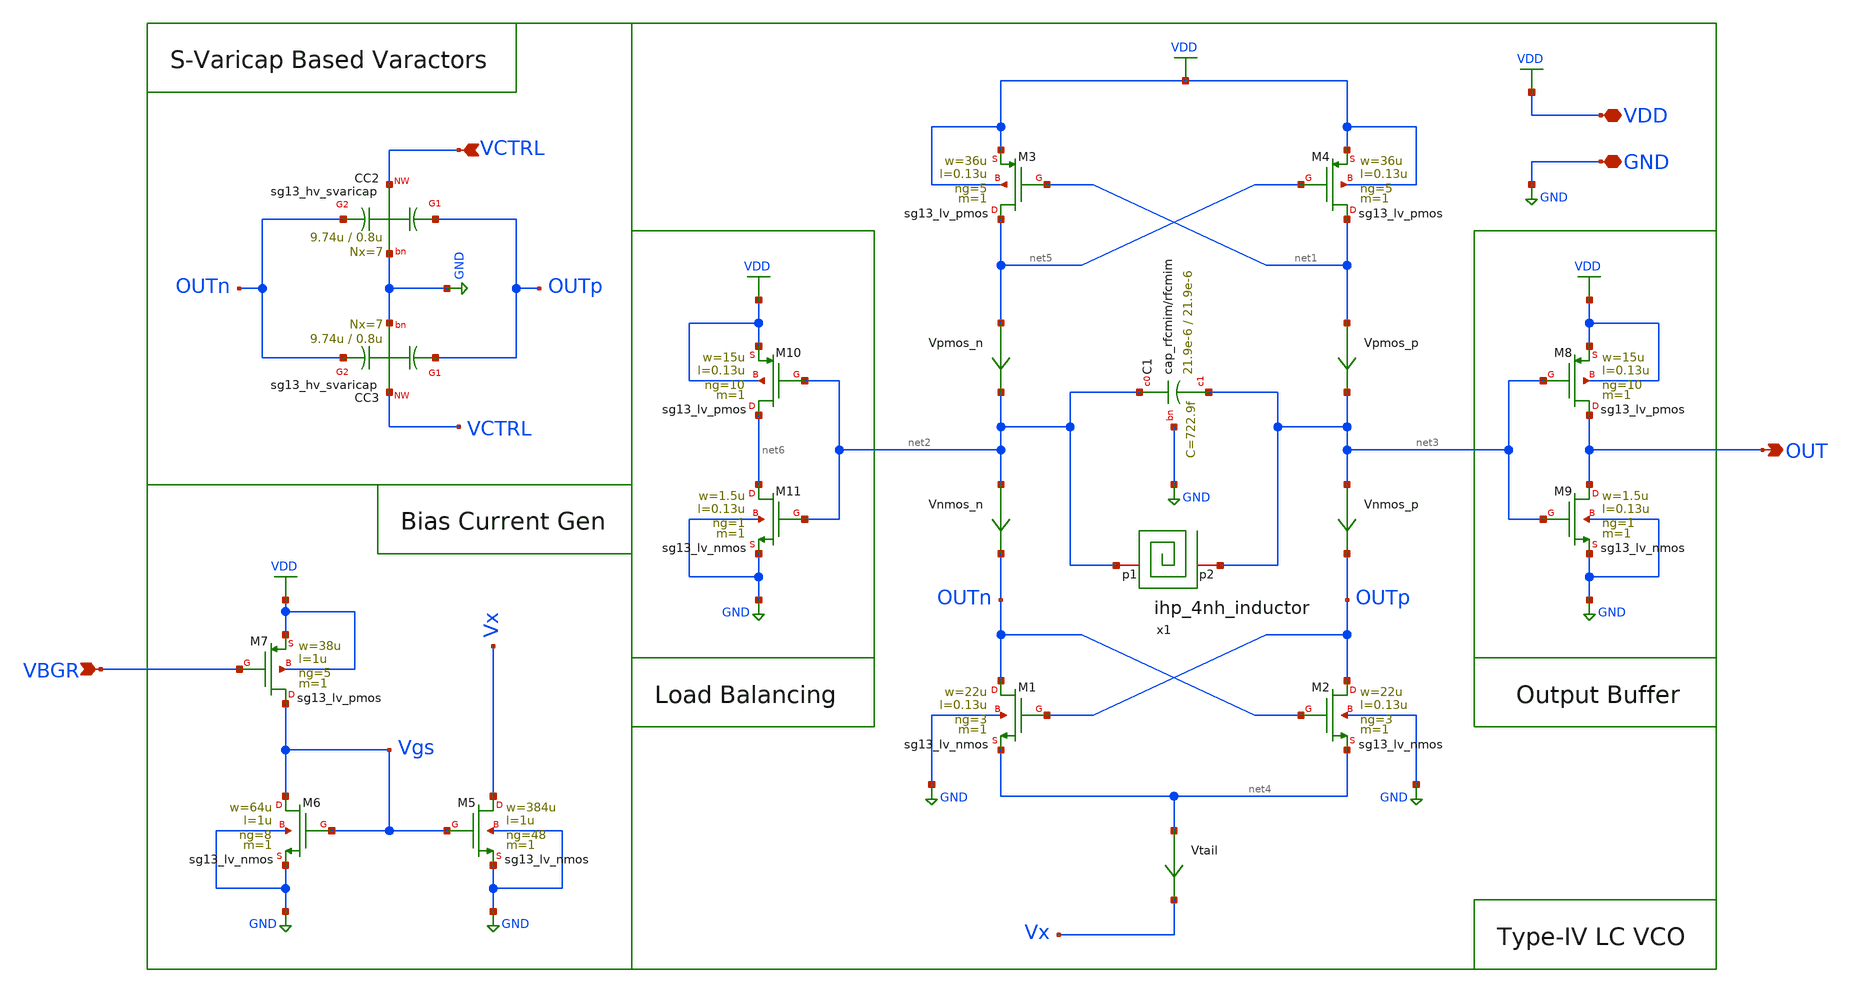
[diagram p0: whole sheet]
** sch_path: xschem/lc-vco/LC_VCO_standalone.sch
**.subckt LC_VCO_standalone OUT VCTRL VBGR VDD GND
*.opin OUT
*.ipin VCTRL
*.ipin VBGR
*.iopin VDD
*.iopin GND
XM5 Vx Vgs GND GND sg13_lv_nmos w=384u l=1u ng=48 m=1 mm_ok=1
XM4 net1 net5 VDD VDD sg13_lv_pmos w=36u l=0.13u ng=5 m=1 mm_ok=1
XM3 net5 net1 VDD VDD sg13_lv_pmos w=36u l=0.13u ng=5 m=1 mm_ok=1
XM2 OUTp OUTn net4 GND sg13_lv_nmos w=22u l=0.13u ng=3 m=1 mm_ok=1
XM1 OUTn OUTp net4 GND sg13_lv_nmos w=22u l=0.13u ng=3 m=1 mm_ok=1
Vpmos_p net1 net3 0
.save i(vpmos_p)
Vnmos_p net3 OUTp 0
.save i(vnmos_p)
Vtail net4 Vx 0
.save i(vtail)
XM6 Vgs Vgs GND GND sg13_lv_nmos w=64u l=1u ng=8 m=1 mm_ok=1
Vpmos_n net5 net2 0
.save i(vpmos_n)
Vnmos_n net2 OUTn 0
.save i(vnmos_n)
x1 net2 net3 ihp_4nh_inductor
XC1 net2 net3 GND cap_rfcmim w=21.9e-6 l=21.9e-6 wfeed=10.0e-6 m=1 mm_ok=1
XC3 OUTp VCTRL OUTn GND sg13_hv_svaricap w=9.74u l=0.8u Nx=7
XC2 OUTp VCTRL OUTn GND sg13_hv_svaricap w=9.74u l=0.8u Nx=7
XM7 Vgs VBGR VDD VDD sg13_lv_pmos w=38u l=1u ng=5 m=1 mm_ok=1
XM8 OUT net3 VDD VDD sg13_lv_pmos w=15u l=0.13u ng=10 m=1 mm_ok=1
XM9 OUT net3 GND GND sg13_lv_nmos w=1.5u l=0.13u ng=1 m=1 mm_ok=1
XM10 net6 net2 VDD VDD sg13_lv_pmos w=15u l=0.13u ng=10 m=1 mm_ok=1
XM11 net6 net2 GND GND sg13_lv_nmos w=1.5u l=0.13u ng=1 m=1 mm_ok=1
**.ends
.GLOBAL GND
.GLOBAL VDD
.end
